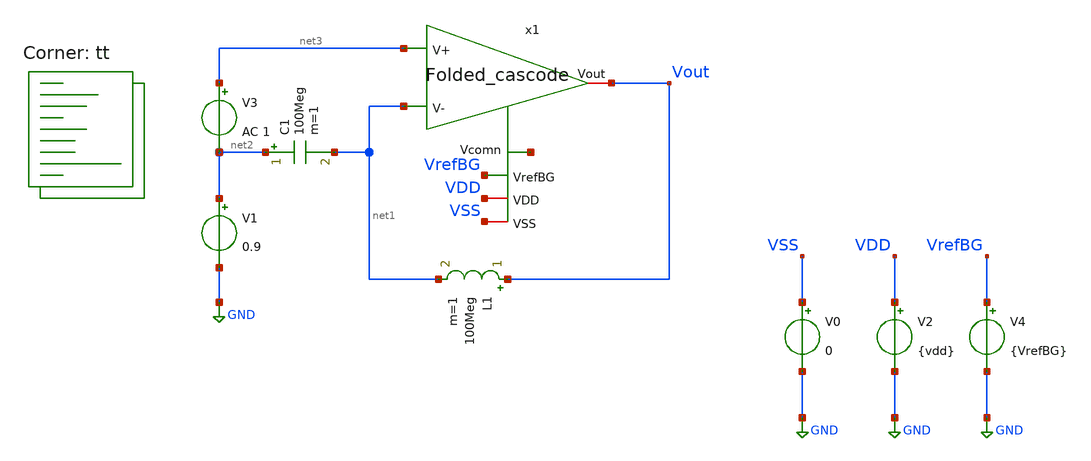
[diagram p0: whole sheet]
** sch_path: openfasoc/generators/curref-gen/sch/Folded_cascode_tb.sch
**.subckt Folded_cascode_tb
V0 VSS GND 0
V2 VDD GND {vdd}
L1 Vout net1 100Meg m=1
V1 net2 GND 0.9
V3 net3 net2 AC 1
C1 net2 net1 100Meg m=1
V4 VrefBG GND {VrefBG}
x1 Vout net3 net1 VrefBG VDD VSS net4 Folded_cascode
**** begin user architecture code
.lib $::SKYWATER_MODELS/sky130.lib.spice tt



.param vdd=1.8
.param VrefBG=1.2

.save

.control

    op
    show

    write Folded_cascode_tb.raw
    set appendwrite

    * run ac simulation
    ac dec 20 1 100e6

    * measure parameters
    let vout_mag = db(abs(v(Vout)))

    meas ac A0 find vout_mag at=1k

    write Folded_cascode_tb.raw
.endc



**** end user architecture code
**.ends

* expanding   symbol:  /foss/designs/Folded_cascode/Folded_cascode.sym # of pins=7
** sym_path: openfasoc/generators/curref-gen/sch/Folded_cascode.sym
** sch_path: openfasoc/generators/curref-gen/sch/Folded_cascode.sch
.subckt Folded_cascode Vout V+ V- VrefBG VDD VSS Vcomn
*.ipin V+
*.ipin V-
*.ipin VrefBG
*.iopin VDD
*.iopin VSS
*.iopin Vout
*.iopin Vcomn
XM6 net2 V- net5 net5 sky130_fd_pr__nfet_01v8 L=1 W=1 nf=1 ad='int((nf+1)/2) * W/nf * 0.29' as='int((nf+2)/2) * W/nf * 0.29'
+ pd='2*int((nf+1)/2) * (W/nf + 0.29)' ps='2*int((nf+2)/2) * (W/nf + 0.29)' nrd='0.29 / W' nrs='0.29 / W'
+ sa=0 sb=0 sd=0 mult=20 m=20
XM7 Vout VB2 Vcomn VSS sky130_fd_pr__nfet_01v8 L=3 W=1 nf=1 ad='int((nf+1)/2) * W/nf * 0.29' as='int((nf+2)/2) * W/nf * 0.29'
+ pd='2*int((nf+1)/2) * (W/nf + 0.29)' ps='2*int((nf+2)/2) * (W/nf + 0.29)' nrd='0.29 / W' nrs='0.29 / W'
+ sa=0 sb=0 sd=0 mult=5 m=5
XM8 net4 VB2 net3 VSS sky130_fd_pr__nfet_01v8 L=3 W=1 nf=1 ad='int((nf+1)/2) * W/nf * 0.29' as='int((nf+2)/2) * W/nf * 0.29'
+ pd='2*int((nf+1)/2) * (W/nf + 0.29)' ps='2*int((nf+2)/2) * (W/nf + 0.29)' nrd='0.29 / W' nrs='0.29 / W'
+ sa=0 sb=0 sd=0 mult=5 m=5
XM9 Vcomn VP VSS VSS sky130_fd_pr__nfet_01v8 L=6.5 W=0.5 nf=1 ad='int((nf+1)/2) * W/nf * 0.29' as='int((nf+2)/2) * W/nf * 0.29'
+ pd='2*int((nf+1)/2) * (W/nf + 0.29)' ps='2*int((nf+2)/2) * (W/nf + 0.29)' nrd='0.29 / W' nrs='0.29 / W'
+ sa=0 sb=0 sd=0 mult=5 m=5
XM10 net3 VP VSS VSS sky130_fd_pr__nfet_01v8 L=6.5 W=0.5 nf=1 ad='int((nf+1)/2) * W/nf * 0.29' as='int((nf+2)/2) * W/nf * 0.29'
+ pd='2*int((nf+1)/2) * (W/nf + 0.29)' ps='2*int((nf+2)/2) * (W/nf + 0.29)' nrd='0.29 / W' nrs='0.29 / W'
+ sa=0 sb=0 sd=0 mult=5 m=5
XM11 net5 VP VSS VSS sky130_fd_pr__nfet_01v8 L=6.5 W=0.5 nf=1 ad='int((nf+1)/2) * W/nf * 0.29' as='int((nf+2)/2) * W/nf * 0.29'
+ pd='2*int((nf+1)/2) * (W/nf + 0.29)' ps='2*int((nf+2)/2) * (W/nf + 0.29)' nrd='0.29 / W' nrs='0.29 / W'
+ sa=0 sb=0 sd=0 mult=10 m=10
XM1 net1 V+ net5 net5 sky130_fd_pr__nfet_01v8 L=1 W=1 nf=1 ad='int((nf+1)/2) * W/nf * 0.29' as='int((nf+2)/2) * W/nf * 0.29'
+ pd='2*int((nf+1)/2) * (W/nf + 0.29)' ps='2*int((nf+2)/2) * (W/nf + 0.29)' nrd='0.29 / W' nrs='0.29 / W'
+ sa=0 sb=0 sd=0 mult=20 m=20
XM12 VP VP VSS VSS sky130_fd_pr__nfet_01v8 L=6.5 W=0.5 nf=1 ad='int((nf+1)/2) * W/nf * 0.29' as='int((nf+2)/2) * W/nf * 0.29'
+ pd='2*int((nf+1)/2) * (W/nf + 0.29)' ps='2*int((nf+2)/2) * (W/nf + 0.29)' nrd='0.29 / W' nrs='0.29 / W'
+ sa=0 sb=0 sd=0 mult=1 m=1
XM13 net6 VP VSS VSS sky130_fd_pr__nfet_01v8 L=6.5 W=0.5 nf=1 ad='int((nf+1)/2) * W/nf * 0.29' as='int((nf+2)/2) * W/nf * 0.29'
+ pd='2*int((nf+1)/2) * (W/nf + 0.29)' ps='2*int((nf+2)/2) * (W/nf + 0.29)' nrd='0.29 / W' nrs='0.29 / W'
+ sa=0 sb=0 sd=0 mult=1 m=1
XM17 VB2 VB2 VSS VSS sky130_fd_pr__nfet_01v8 L=18 W=0.42 nf=1 ad='int((nf+1)/2) * W/nf * 0.29' as='int((nf+2)/2) * W/nf * 0.29'
+ pd='2*int((nf+1)/2) * (W/nf + 0.29)' ps='2*int((nf+2)/2) * (W/nf + 0.29)' nrd='0.29 / W' nrs='0.29 / W'
+ sa=0 sb=0 sd=0 mult=1 m=1
XM18 VB2 net6 VDD VDD sky130_fd_pr__pfet_01v8_lvt L=6 W=0.5 nf=1 ad='int((1 + 1)/2) * 0.5 / 1 * 0.29'
+ as='int((1 + 2)/2) * 0.5 / 1 * 0.29' pd='2*int((1 + 1)/2) * (0.5 / 1 + 0.29)' ps='2*int((1 + 2)/2) * (0.5 / 1 + 0.29)'
+ nrd='0.29 / 0.5 ' nrs='0.29 / 0.5 ' sa=0 sb=0 sd=0 mult=4 m=4
XM15 net6 net6 VDD VDD sky130_fd_pr__pfet_01v8_lvt L=6 W=0.5 nf=1 ad='int((1 + 1)/2) * 0.5 / 1 * 0.29'
+ as='int((1 + 2)/2) * 0.5 / 1 * 0.29' pd='2*int((1 + 1)/2) * (0.5 / 1 + 0.29)' ps='2*int((1 + 2)/2) * (0.5 / 1 + 0.29)'
+ nrd='0.29 / 0.5 ' nrs='0.29 / 0.5 ' sa=0 sb=0 sd=0 mult=4 m=4
XM3 net1 net4 VDD VDD sky130_fd_pr__pfet_01v8_lvt L=3 W=1 nf=1 ad='int((1 + 1)/2) * 1 / 1 * 0.29' as='int((1 + 2)/2) * 1 / 1 * 0.29'
+ pd='2*int((1 + 1)/2) * (1 / 1 + 0.29)' ps='2*int((1 + 2)/2) * (1 / 1 + 0.29)' nrd='0.29 / 1 ' nrs='0.29 / 1 '
+ sa=0 sb=0 sd=0 mult=6 m=6
XM2 net2 net4 VDD VDD sky130_fd_pr__pfet_01v8_lvt L=3 W=1 nf=1 ad='int((1 + 1)/2) * 1 / 1 * 0.29' as='int((1 + 2)/2) * 1 / 1 * 0.29'
+ pd='2*int((1 + 1)/2) * (1 / 1 + 0.29)' ps='2*int((1 + 2)/2) * (1 / 1 + 0.29)' nrd='0.29 / 1 ' nrs='0.29 / 1 '
+ sa=0 sb=0 sd=0 mult=6 m=6
XM5 net4 VB1 net1 VDD sky130_fd_pr__pfet_01v8_lvt L=1.5 W=1 nf=1 ad='int((1 + 1)/2) * 1 / 1 * 0.29' as='int((1 + 2)/2) * 1 / 1 * 0.29'
+ pd='2*int((1 + 1)/2) * (1 / 1 + 0.29)' ps='2*int((1 + 2)/2) * (1 / 1 + 0.29)' nrd='0.29 / 1 ' nrs='0.29 / 1 '
+ sa=0 sb=0 sd=0 mult=10 m=10
XM16 Vout VB1 net2 VDD sky130_fd_pr__pfet_01v8_lvt L=1.5 W=1 nf=1 ad='int((1 + 1)/2) * 1 / 1 * 0.29'
+ as='int((1 + 2)/2) * 1 / 1 * 0.29' pd='2*int((1 + 1)/2) * (1 / 1 + 0.29)' ps='2*int((1 + 2)/2) * (1 / 1 + 0.29)'
+ nrd='0.29 / 1 ' nrs='0.29 / 1 ' sa=0 sb=0 sd=0 mult=10 m=10
XM4 VP VB1 VDD VDD sky130_fd_pr__pfet_01v8_lvt L=6 W=0.5 nf=1 ad='int((1 + 1)/2) * 0.5 / 1 * 0.29' as='int((1 + 2)/2) * 0.5 / 1 * 0.29'
+ pd='2*int((1 + 1)/2) * (0.5 / 1 + 0.29)' ps='2*int((1 + 2)/2) * (0.5 / 1 + 0.29)' nrd='0.29 / 0.5 ' nrs='0.29 / 0.5 '
+ sa=0 sb=0 sd=0 mult=1 m=1
XM14 VB1 VB1 VDD VDD sky130_fd_pr__pfet_01v8_lvt L=6 W=0.5 nf=1 ad='int((1 + 1)/2) * 0.5 / 1 * 0.29'
+ as='int((1 + 2)/2) * 0.5 / 1 * 0.29' pd='2*int((1 + 1)/2) * (0.5 / 1 + 0.29)' ps='2*int((1 + 2)/2) * (0.5 / 1 + 0.29)'
+ nrd='0.29 / 0.5 ' nrs='0.29 / 0.5 ' sa=0 sb=0 sd=0 mult=1 m=1
XM19 VB1 VrefBG VSS VSS sky130_fd_pr__nfet_01v8 L=18 W=0.45 nf=1 ad='int((nf+1)/2) * W/nf * 0.29' as='int((nf+2)/2) * W/nf * 0.29'
+ pd='2*int((nf+1)/2) * (W/nf + 0.29)' ps='2*int((nf+2)/2) * (W/nf + 0.29)' nrd='0.29 / W' nrs='0.29 / W'
+ sa=0 sb=0 sd=0 mult=1 m=1
.ends

.GLOBAL GND
.end
